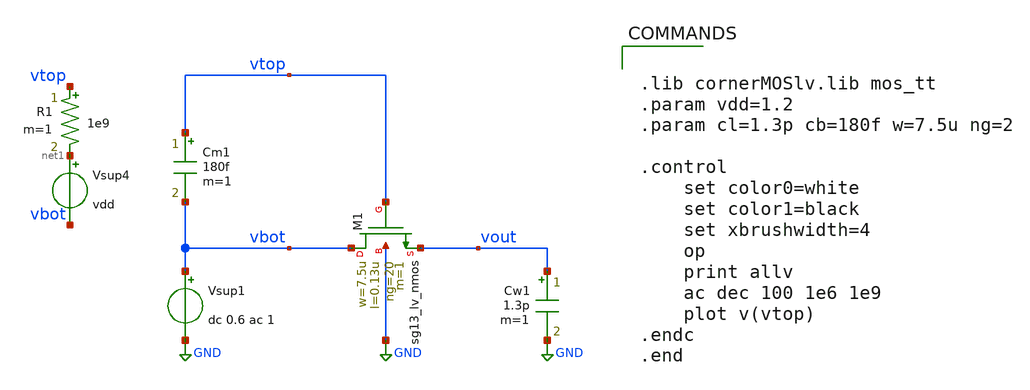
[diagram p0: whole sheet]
** sch_path: xschem/tb_boot1_csmall.sch
**.subckt tb_boot1_csmall
Cw1 vout GND 1.3p m=1
Vsup1 vbot GND dc 0.6 ac 1
Cm1 vtop vbot 180f m=1
XM1 vbot vtop vout GND sg13_lv_nmos w=7.5u l=0.13u ng=20 m=1 mm_ok=1
Vsup4 net1 vbot vdd
R1 vtop net1 1e9 m=1
**** begin user architecture code


.lib cornerMOSlv.lib mos_tt
.param vdd=1.2
.param cl=1.3p cb=180f w=7.5u ng=2

.control
    set color0=white
    set color1=black
    set xbrushwidth=4
    op
    print allv
    ac dec 100 1e6 1e9
    plot v(vtop)
.endc
.end


**** end user architecture code
**.ends
.GLOBAL GND
.end
